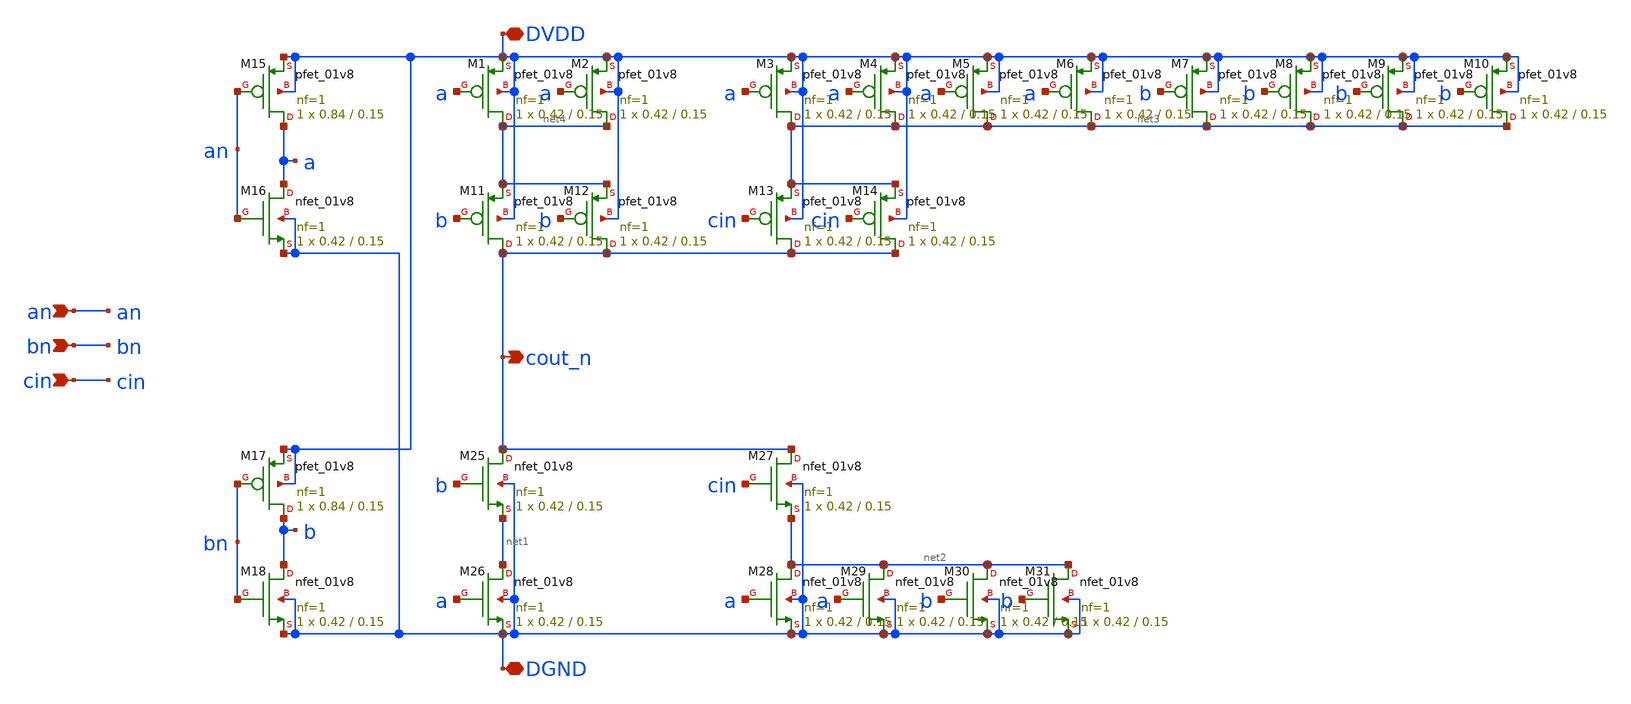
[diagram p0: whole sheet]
** sch_path: tut6/again_lf/carry/carry.sch
**.subckt carry an bn cin DGND DVDD cout_n
*.ipin an
*.ipin bn
*.ipin cin
*.iopin DGND
*.iopin DVDD
*.opin cout_n
XM1 net4 a DVDD DVDD sky130_fd_pr__pfet_01v8 L=0.15 W=0.42 nf=1 ad='int((nf+1)/2) * W/nf * 0.29' as='int((nf+2)/2) * W/nf * 0.29'
+ pd='2*int((nf+1)/2) * (W/nf + 0.29)' ps='2*int((nf+2)/2) * (W/nf + 0.29)' nrd='0.29 / W' nrs='0.29 / W'
+ sa=0 sb=0 sd=0 mult=1 m=1
XM2 net4 a DVDD DVDD sky130_fd_pr__pfet_01v8 L=0.15 W=0.42 nf=1 ad='int((nf+1)/2) * W/nf * 0.29' as='int((nf+2)/2) * W/nf * 0.29'
+ pd='2*int((nf+1)/2) * (W/nf + 0.29)' ps='2*int((nf+2)/2) * (W/nf + 0.29)' nrd='0.29 / W' nrs='0.29 / W'
+ sa=0 sb=0 sd=0 mult=1 m=1
XM3 net3 a DVDD DVDD sky130_fd_pr__pfet_01v8 L=0.15 W=0.42 nf=1 ad='int((nf+1)/2) * W/nf * 0.29' as='int((nf+2)/2) * W/nf * 0.29'
+ pd='2*int((nf+1)/2) * (W/nf + 0.29)' ps='2*int((nf+2)/2) * (W/nf + 0.29)' nrd='0.29 / W' nrs='0.29 / W'
+ sa=0 sb=0 sd=0 mult=1 m=1
XM4 net3 a DVDD DVDD sky130_fd_pr__pfet_01v8 L=0.15 W=0.42 nf=1 ad='int((nf+1)/2) * W/nf * 0.29' as='int((nf+2)/2) * W/nf * 0.29'
+ pd='2*int((nf+1)/2) * (W/nf + 0.29)' ps='2*int((nf+2)/2) * (W/nf + 0.29)' nrd='0.29 / W' nrs='0.29 / W'
+ sa=0 sb=0 sd=0 mult=1 m=1
XM11 cout_n b net4 DVDD sky130_fd_pr__pfet_01v8 L=0.15 W=0.42 nf=1 ad='int((nf+1)/2) * W/nf * 0.29' as='int((nf+2)/2) * W/nf * 0.29'
+ pd='2*int((nf+1)/2) * (W/nf + 0.29)' ps='2*int((nf+2)/2) * (W/nf + 0.29)' nrd='0.29 / W' nrs='0.29 / W'
+ sa=0 sb=0 sd=0 mult=1 m=1
XM12 cout_n b net4 DVDD sky130_fd_pr__pfet_01v8 L=0.15 W=0.42 nf=1 ad='int((nf+1)/2) * W/nf * 0.29' as='int((nf+2)/2) * W/nf * 0.29'
+ pd='2*int((nf+1)/2) * (W/nf + 0.29)' ps='2*int((nf+2)/2) * (W/nf + 0.29)' nrd='0.29 / W' nrs='0.29 / W'
+ sa=0 sb=0 sd=0 mult=1 m=1
XM13 cout_n cin net3 DVDD sky130_fd_pr__pfet_01v8 L=0.15 W=0.42 nf=1 ad='int((nf+1)/2) * W/nf * 0.29'
+ as='int((nf+2)/2) * W/nf * 0.29' pd='2*int((nf+1)/2) * (W/nf + 0.29)' ps='2*int((nf+2)/2) * (W/nf + 0.29)'
+ nrd='0.29 / W' nrs='0.29 / W' sa=0 sb=0 sd=0 mult=1 m=1
XM14 cout_n cin net3 DVDD sky130_fd_pr__pfet_01v8 L=0.15 W=0.42 nf=1 ad='int((nf+1)/2) * W/nf * 0.29'
+ as='int((nf+2)/2) * W/nf * 0.29' pd='2*int((nf+1)/2) * (W/nf + 0.29)' ps='2*int((nf+2)/2) * (W/nf + 0.29)'
+ nrd='0.29 / W' nrs='0.29 / W' sa=0 sb=0 sd=0 mult=1 m=1
XM25 cout_n b net1 DGND sky130_fd_pr__nfet_01v8 L=0.15 W=0.42 nf=1 ad='int((nf+1)/2) * W/nf * 0.29' as='int((nf+2)/2) * W/nf * 0.29'
+ pd='2*int((nf+1)/2) * (W/nf + 0.29)' ps='2*int((nf+2)/2) * (W/nf + 0.29)' nrd='0.29 / W' nrs='0.29 / W'
+ sa=0 sb=0 sd=0 mult=1 m=1
XM26 net1 a DGND DGND sky130_fd_pr__nfet_01v8 L=0.15 W=0.42 nf=1 ad='int((nf+1)/2) * W/nf * 0.29' as='int((nf+2)/2) * W/nf * 0.29'
+ pd='2*int((nf+1)/2) * (W/nf + 0.29)' ps='2*int((nf+2)/2) * (W/nf + 0.29)' nrd='0.29 / W' nrs='0.29 / W'
+ sa=0 sb=0 sd=0 mult=1 m=1
XM27 cout_n cin net2 DGND sky130_fd_pr__nfet_01v8 L=0.15 W=0.42 nf=1 ad='int((nf+1)/2) * W/nf * 0.29'
+ as='int((nf+2)/2) * W/nf * 0.29' pd='2*int((nf+1)/2) * (W/nf + 0.29)' ps='2*int((nf+2)/2) * (W/nf + 0.29)'
+ nrd='0.29 / W' nrs='0.29 / W' sa=0 sb=0 sd=0 mult=1 m=1
XM28 net2 a DGND DGND sky130_fd_pr__nfet_01v8 L=0.15 W=0.42 nf=1 ad='int((nf+1)/2) * W/nf * 0.29' as='int((nf+2)/2) * W/nf * 0.29'
+ pd='2*int((nf+1)/2) * (W/nf + 0.29)' ps='2*int((nf+2)/2) * (W/nf + 0.29)' nrd='0.29 / W' nrs='0.29 / W'
+ sa=0 sb=0 sd=0 mult=1 m=1
XM5 net3 a DVDD DVDD sky130_fd_pr__pfet_01v8 L=0.15 W=0.42 nf=1 ad='int((nf+1)/2) * W/nf * 0.29' as='int((nf+2)/2) * W/nf * 0.29'
+ pd='2*int((nf+1)/2) * (W/nf + 0.29)' ps='2*int((nf+2)/2) * (W/nf + 0.29)' nrd='0.29 / W' nrs='0.29 / W'
+ sa=0 sb=0 sd=0 mult=1 m=1
XM6 net3 a DVDD DVDD sky130_fd_pr__pfet_01v8 L=0.15 W=0.42 nf=1 ad='int((nf+1)/2) * W/nf * 0.29' as='int((nf+2)/2) * W/nf * 0.29'
+ pd='2*int((nf+1)/2) * (W/nf + 0.29)' ps='2*int((nf+2)/2) * (W/nf + 0.29)' nrd='0.29 / W' nrs='0.29 / W'
+ sa=0 sb=0 sd=0 mult=1 m=1
XM7 net3 b DVDD DVDD sky130_fd_pr__pfet_01v8 L=0.15 W=0.42 nf=1 ad='int((nf+1)/2) * W/nf * 0.29' as='int((nf+2)/2) * W/nf * 0.29'
+ pd='2*int((nf+1)/2) * (W/nf + 0.29)' ps='2*int((nf+2)/2) * (W/nf + 0.29)' nrd='0.29 / W' nrs='0.29 / W'
+ sa=0 sb=0 sd=0 mult=1 m=1
XM8 net3 b DVDD DVDD sky130_fd_pr__pfet_01v8 L=0.15 W=0.42 nf=1 ad='int((nf+1)/2) * W/nf * 0.29' as='int((nf+2)/2) * W/nf * 0.29'
+ pd='2*int((nf+1)/2) * (W/nf + 0.29)' ps='2*int((nf+2)/2) * (W/nf + 0.29)' nrd='0.29 / W' nrs='0.29 / W'
+ sa=0 sb=0 sd=0 mult=1 m=1
XM9 net3 b DVDD DVDD sky130_fd_pr__pfet_01v8 L=0.15 W=0.42 nf=1 ad='int((nf+1)/2) * W/nf * 0.29' as='int((nf+2)/2) * W/nf * 0.29'
+ pd='2*int((nf+1)/2) * (W/nf + 0.29)' ps='2*int((nf+2)/2) * (W/nf + 0.29)' nrd='0.29 / W' nrs='0.29 / W'
+ sa=0 sb=0 sd=0 mult=1 m=1
XM10 net3 b DVDD DVDD sky130_fd_pr__pfet_01v8 L=0.15 W=0.42 nf=1 ad='int((nf+1)/2) * W/nf * 0.29' as='int((nf+2)/2) * W/nf * 0.29'
+ pd='2*int((nf+1)/2) * (W/nf + 0.29)' ps='2*int((nf+2)/2) * (W/nf + 0.29)' nrd='0.29 / W' nrs='0.29 / W'
+ sa=0 sb=0 sd=0 mult=1 m=1
XM29 net2 a DGND DGND sky130_fd_pr__nfet_01v8 L=0.15 W=0.42 nf=1 ad='int((nf+1)/2) * W/nf * 0.29' as='int((nf+2)/2) * W/nf * 0.29'
+ pd='2*int((nf+1)/2) * (W/nf + 0.29)' ps='2*int((nf+2)/2) * (W/nf + 0.29)' nrd='0.29 / W' nrs='0.29 / W'
+ sa=0 sb=0 sd=0 mult=1 m=1
XM30 net2 b DGND DGND sky130_fd_pr__nfet_01v8 L=0.15 W=0.42 nf=1 ad='int((nf+1)/2) * W/nf * 0.29' as='int((nf+2)/2) * W/nf * 0.29'
+ pd='2*int((nf+1)/2) * (W/nf + 0.29)' ps='2*int((nf+2)/2) * (W/nf + 0.29)' nrd='0.29 / W' nrs='0.29 / W'
+ sa=0 sb=0 sd=0 mult=1 m=1
XM31 net2 b DGND DGND sky130_fd_pr__nfet_01v8 L=0.15 W=0.42 nf=1 ad='int((nf+1)/2) * W/nf * 0.29' as='int((nf+2)/2) * W/nf * 0.29'
+ pd='2*int((nf+1)/2) * (W/nf + 0.29)' ps='2*int((nf+2)/2) * (W/nf + 0.29)' nrd='0.29 / W' nrs='0.29 / W'
+ sa=0 sb=0 sd=0 mult=1 m=1
XM15 a an DVDD DVDD sky130_fd_pr__pfet_01v8 L=0.15 W=0.84 nf=1 ad='int((nf+1)/2) * W/nf * 0.29' as='int((nf+2)/2) * W/nf * 0.29'
+ pd='2*int((nf+1)/2) * (W/nf + 0.29)' ps='2*int((nf+2)/2) * (W/nf + 0.29)' nrd='0.29 / W' nrs='0.29 / W'
+ sa=0 sb=0 sd=0 mult=1 m=1
XM16 a an DGND DGND sky130_fd_pr__nfet_01v8 L=0.15 W=0.42 nf=1 ad='int((nf+1)/2) * W/nf * 0.29' as='int((nf+2)/2) * W/nf * 0.29'
+ pd='2*int((nf+1)/2) * (W/nf + 0.29)' ps='2*int((nf+2)/2) * (W/nf + 0.29)' nrd='0.29 / W' nrs='0.29 / W'
+ sa=0 sb=0 sd=0 mult=1 m=1
XM17 b bn DVDD DVDD sky130_fd_pr__pfet_01v8 L=0.15 W=0.84 nf=1 ad='int((nf+1)/2) * W/nf * 0.29' as='int((nf+2)/2) * W/nf * 0.29'
+ pd='2*int((nf+1)/2) * (W/nf + 0.29)' ps='2*int((nf+2)/2) * (W/nf + 0.29)' nrd='0.29 / W' nrs='0.29 / W'
+ sa=0 sb=0 sd=0 mult=1 m=1
XM18 b bn DGND DGND sky130_fd_pr__nfet_01v8 L=0.15 W=0.42 nf=1 ad='int((nf+1)/2) * W/nf * 0.29' as='int((nf+2)/2) * W/nf * 0.29'
+ pd='2*int((nf+1)/2) * (W/nf + 0.29)' ps='2*int((nf+2)/2) * (W/nf + 0.29)' nrd='0.29 / W' nrs='0.29 / W'
+ sa=0 sb=0 sd=0 mult=1 m=1
**.ends
.end
